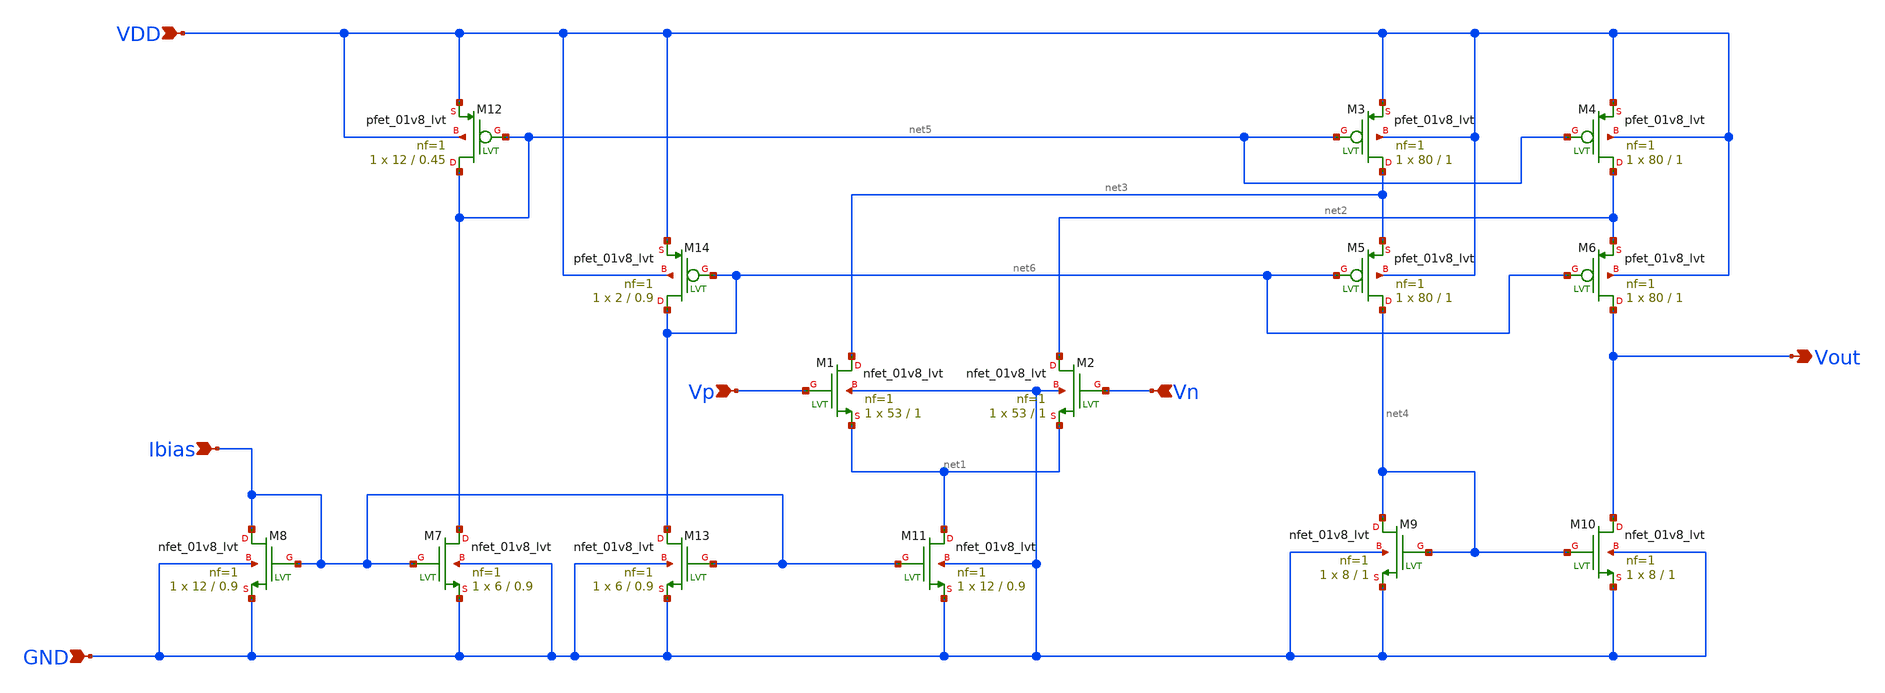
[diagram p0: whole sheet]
** sch_path: Analog_Blocks/OTA/Schematic/Folded_Cascode_OTA/Transistor1.8v/Folded_Cascode_OTA.sch
**.subckt Folded_Cascode_OTA VDD GND Vp Vn Vout Ibias
*.ipin VDD
*.ipin GND
*.ipin Vp
*.ipin Vn
*.opin Vout
*.ipin Ibias
XM1 net3 Vp net1 GND sky130_fd_pr__nfet_01v8_lvt L=1 W=53 nf=1 ad='int((nf+1)/2) * W/nf * 0.29' as='int((nf+2)/2) * W/nf * 0.29'
+ pd='2*int((nf+1)/2) * (W/nf + 0.29)' ps='2*int((nf+2)/2) * (W/nf + 0.29)' nrd='0.29 / W' nrs='0.29 / W'
+ sa=0 sb=0 sd=0 mult=1 m=1
XM2 net2 Vn net1 GND sky130_fd_pr__nfet_01v8_lvt L=1 W=53 nf=1 ad='int((nf+1)/2) * W/nf * 0.29' as='int((nf+2)/2) * W/nf * 0.29'
+ pd='2*int((nf+1)/2) * (W/nf + 0.29)' ps='2*int((nf+2)/2) * (W/nf + 0.29)' nrd='0.29 / W' nrs='0.29 / W'
+ sa=0 sb=0 sd=0 mult=1 m=1
XM3 net3 net5 VDD VDD sky130_fd_pr__pfet_01v8_lvt L=1 W=80 nf=1 ad='int((nf+1)/2) * W/nf * 0.29' as='int((nf+2)/2) * W/nf * 0.29'
+ pd='2*int((nf+1)/2) * (W/nf + 0.29)' ps='2*int((nf+2)/2) * (W/nf + 0.29)' nrd='0.29 / W' nrs='0.29 / W'
+ sa=0 sb=0 sd=0 mult=1 m=1
XM4 net2 net5 VDD VDD sky130_fd_pr__pfet_01v8_lvt L=1 W=80 nf=1 ad='int((nf+1)/2) * W/nf * 0.29' as='int((nf+2)/2) * W/nf * 0.29'
+ pd='2*int((nf+1)/2) * (W/nf + 0.29)' ps='2*int((nf+2)/2) * (W/nf + 0.29)' nrd='0.29 / W' nrs='0.29 / W'
+ sa=0 sb=0 sd=0 mult=1 m=1
XM5 net4 net6 net3 VDD sky130_fd_pr__pfet_01v8_lvt L=1 W=80 nf=1 ad='int((nf+1)/2) * W/nf * 0.29' as='int((nf+2)/2) * W/nf * 0.29'
+ pd='2*int((nf+1)/2) * (W/nf + 0.29)' ps='2*int((nf+2)/2) * (W/nf + 0.29)' nrd='0.29 / W' nrs='0.29 / W'
+ sa=0 sb=0 sd=0 mult=1 m=1
XM6 Vout net6 net2 VDD sky130_fd_pr__pfet_01v8_lvt L=1 W=80 nf=1 ad='int((nf+1)/2) * W/nf * 0.29' as='int((nf+2)/2) * W/nf * 0.29'
+ pd='2*int((nf+1)/2) * (W/nf + 0.29)' ps='2*int((nf+2)/2) * (W/nf + 0.29)' nrd='0.29 / W' nrs='0.29 / W'
+ sa=0 sb=0 sd=0 mult=1 m=1
XM9 net4 net4 GND GND sky130_fd_pr__nfet_01v8_lvt L=1 W=8 nf=1 ad='int((nf+1)/2) * W/nf * 0.29' as='int((nf+2)/2) * W/nf * 0.29'
+ pd='2*int((nf+1)/2) * (W/nf + 0.29)' ps='2*int((nf+2)/2) * (W/nf + 0.29)' nrd='0.29 / W' nrs='0.29 / W'
+ sa=0 sb=0 sd=0 mult=1 m=1
XM10 Vout net4 GND GND sky130_fd_pr__nfet_01v8_lvt L=1 W=8 nf=1 ad='int((nf+1)/2) * W/nf * 0.29' as='int((nf+2)/2) * W/nf * 0.29'
+ pd='2*int((nf+1)/2) * (W/nf + 0.29)' ps='2*int((nf+2)/2) * (W/nf + 0.29)' nrd='0.29 / W' nrs='0.29 / W'
+ sa=0 sb=0 sd=0 mult=1 m=1
XM11 net1 Ibias GND GND sky130_fd_pr__nfet_01v8_lvt L=0.9 W=12 nf=1 ad='int((nf+1)/2) * W/nf * 0.29'
+ as='int((nf+2)/2) * W/nf * 0.29' pd='2*int((nf+1)/2) * (W/nf + 0.29)' ps='2*int((nf+2)/2) * (W/nf + 0.29)'
+ nrd='0.29 / W' nrs='0.29 / W' sa=0 sb=0 sd=0 mult=1 m=1
XM7 net5 Ibias GND GND sky130_fd_pr__nfet_01v8_lvt L=0.9 W=6 nf=1 ad='int((nf+1)/2) * W/nf * 0.29' as='int((nf+2)/2) * W/nf * 0.29'
+ pd='2*int((nf+1)/2) * (W/nf + 0.29)' ps='2*int((nf+2)/2) * (W/nf + 0.29)' nrd='0.29 / W' nrs='0.29 / W'
+ sa=0 sb=0 sd=0 mult=1 m=1
XM8 Ibias Ibias GND GND sky130_fd_pr__nfet_01v8_lvt L=0.9 W=12 nf=1 ad='int((nf+1)/2) * W/nf * 0.29'
+ as='int((nf+2)/2) * W/nf * 0.29' pd='2*int((nf+1)/2) * (W/nf + 0.29)' ps='2*int((nf+2)/2) * (W/nf + 0.29)'
+ nrd='0.29 / W' nrs='0.29 / W' sa=0 sb=0 sd=0 mult=1 m=1
XM12 net5 net5 VDD VDD sky130_fd_pr__pfet_01v8_lvt L=0.45 W=12 nf=1 ad='int((nf+1)/2) * W/nf * 0.29'
+ as='int((nf+2)/2) * W/nf * 0.29' pd='2*int((nf+1)/2) * (W/nf + 0.29)' ps='2*int((nf+2)/2) * (W/nf + 0.29)'
+ nrd='0.29 / W' nrs='0.29 / W' sa=0 sb=0 sd=0 mult=1 m=1
XM13 net6 Ibias GND GND sky130_fd_pr__nfet_01v8_lvt L=0.9 W=6 nf=1 ad='int((nf+1)/2) * W/nf * 0.29' as='int((nf+2)/2) * W/nf * 0.29'
+ pd='2*int((nf+1)/2) * (W/nf + 0.29)' ps='2*int((nf+2)/2) * (W/nf + 0.29)' nrd='0.29 / W' nrs='0.29 / W'
+ sa=0 sb=0 sd=0 mult=1 m=1
XM14 net6 net6 VDD VDD sky130_fd_pr__pfet_01v8_lvt L=0.9 W=2 nf=1 ad='int((nf+1)/2) * W/nf * 0.29' as='int((nf+2)/2) * W/nf * 0.29'
+ pd='2*int((nf+1)/2) * (W/nf + 0.29)' ps='2*int((nf+2)/2) * (W/nf + 0.29)' nrd='0.29 / W' nrs='0.29 / W'
+ sa=0 sb=0 sd=0 mult=1 m=1
**.ends
.end
